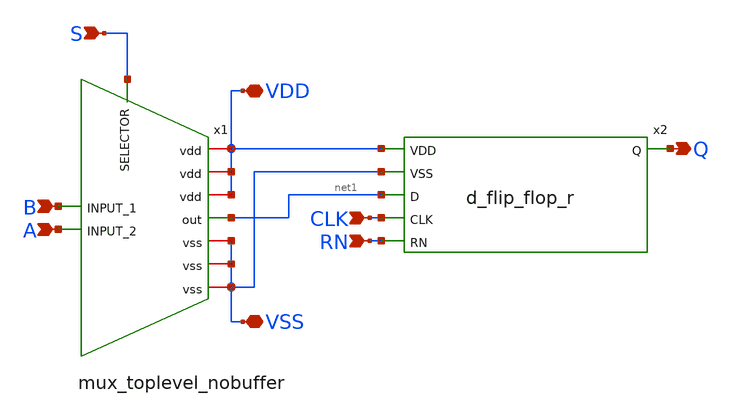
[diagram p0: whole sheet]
** sch_path: designs/libs/core_digital/sddfrnq_tg_nobuffer_toplevel/sdffrq_tg_nobuffer_toplevel.sch
**.subckt sdffrq_tg_nobuffer_toplevel A B S VDD VSS Q RN CLK
*.ipin A
*.ipin B
*.ipin S
*.iopin VDD
*.iopin VSS
*.opin Q
*.ipin RN
*.ipin CLK
x2 VDD VSS Q net1 CLK RN d_flip_flop_r
x1 VDD B VSS net1 A S mux_toplevel_nobuffer
**.ends
.end
